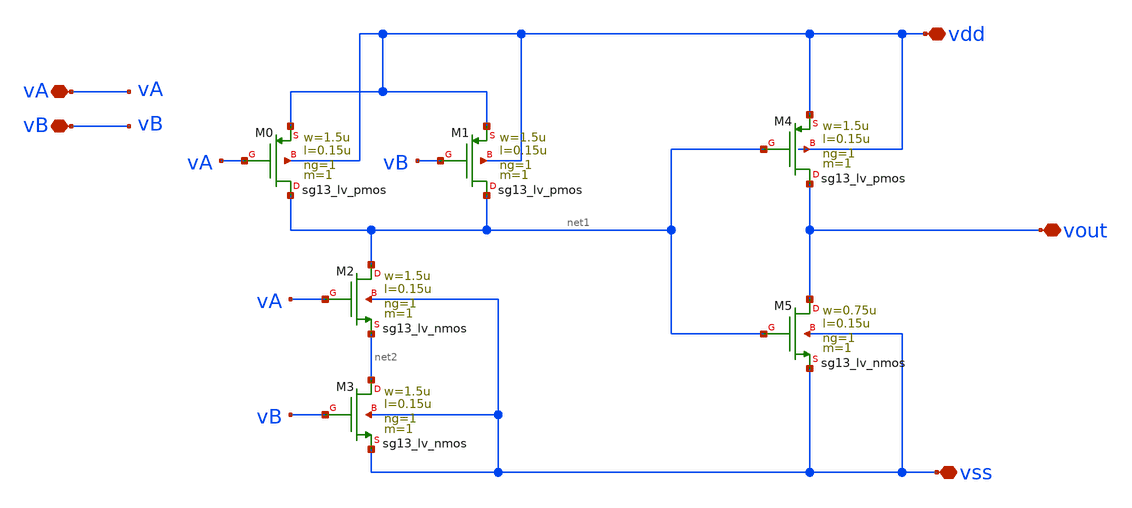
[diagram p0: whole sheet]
** sch_path: design/blocks/andgate/andgate.sch
**.subckt andgate vout vA vB vdd vss
*.iopin vout
*.iopin vA
*.iopin vB
*.iopin vdd
*.iopin vss
XM2 net1 vA net2 vss sg13_lv_nmos w=1.5u l=0.15u ng=1 m=1 mm_ok=1
XM0 net1 vA vdd vdd sg13_lv_pmos w=1.5u l=0.15u ng=1 m=1 mm_ok=1
XM3 net2 vB vss vss sg13_lv_nmos w=1.5u l=0.15u ng=1 m=1 mm_ok=1
XM1 net1 vB vdd vdd sg13_lv_pmos w=1.5u l=0.15u ng=1 m=1 mm_ok=1
XM4 vout net1 vdd vdd sg13_lv_pmos w=1.5u l=0.15u ng=1 m=1 mm_ok=1
XM5 vout net1 vss vss sg13_lv_nmos w=0.75u l=0.15u ng=1 m=1 mm_ok=1
**.ends
.end
